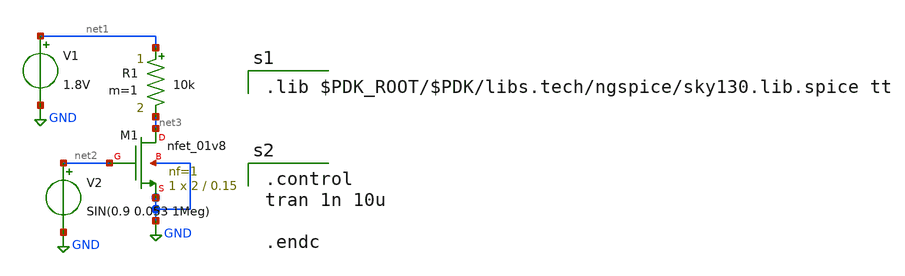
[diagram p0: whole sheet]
** sch_path: schematics/sky130_common_source_amp_transient.sch
**.subckt sky130_common_source_amp_transient
R1 net1 net3 10k m=1
XM1 net3 net2 GND GND sky130_fd_pr__nfet_01v8 L=0.15 W=2 nf=1 ad='int((nf+1)/2) * W/nf * 0.29' as='int((nf+2)/2) * W/nf * 0.29'
+ pd='2*int((nf+1)/2) * (W/nf + 0.29)' ps='2*int((nf+2)/2) * (W/nf + 0.29)' nrd='0.29 / W' nrs='0.29 / W'
+ sa=0 sb=0 sd=0 mult=1 m=1
V1 net1 GND 1.8V
V2 net2 GND SIN(0.9 0.053 1Meg)
**** begin user architecture code

.lib $PDK_ROOT/$PDK/libs.tech/ngspice/sky130.lib.spice tt


.control
tran 1n 10u

.endc

**** end user architecture code
**.ends
.GLOBAL GND
.end
